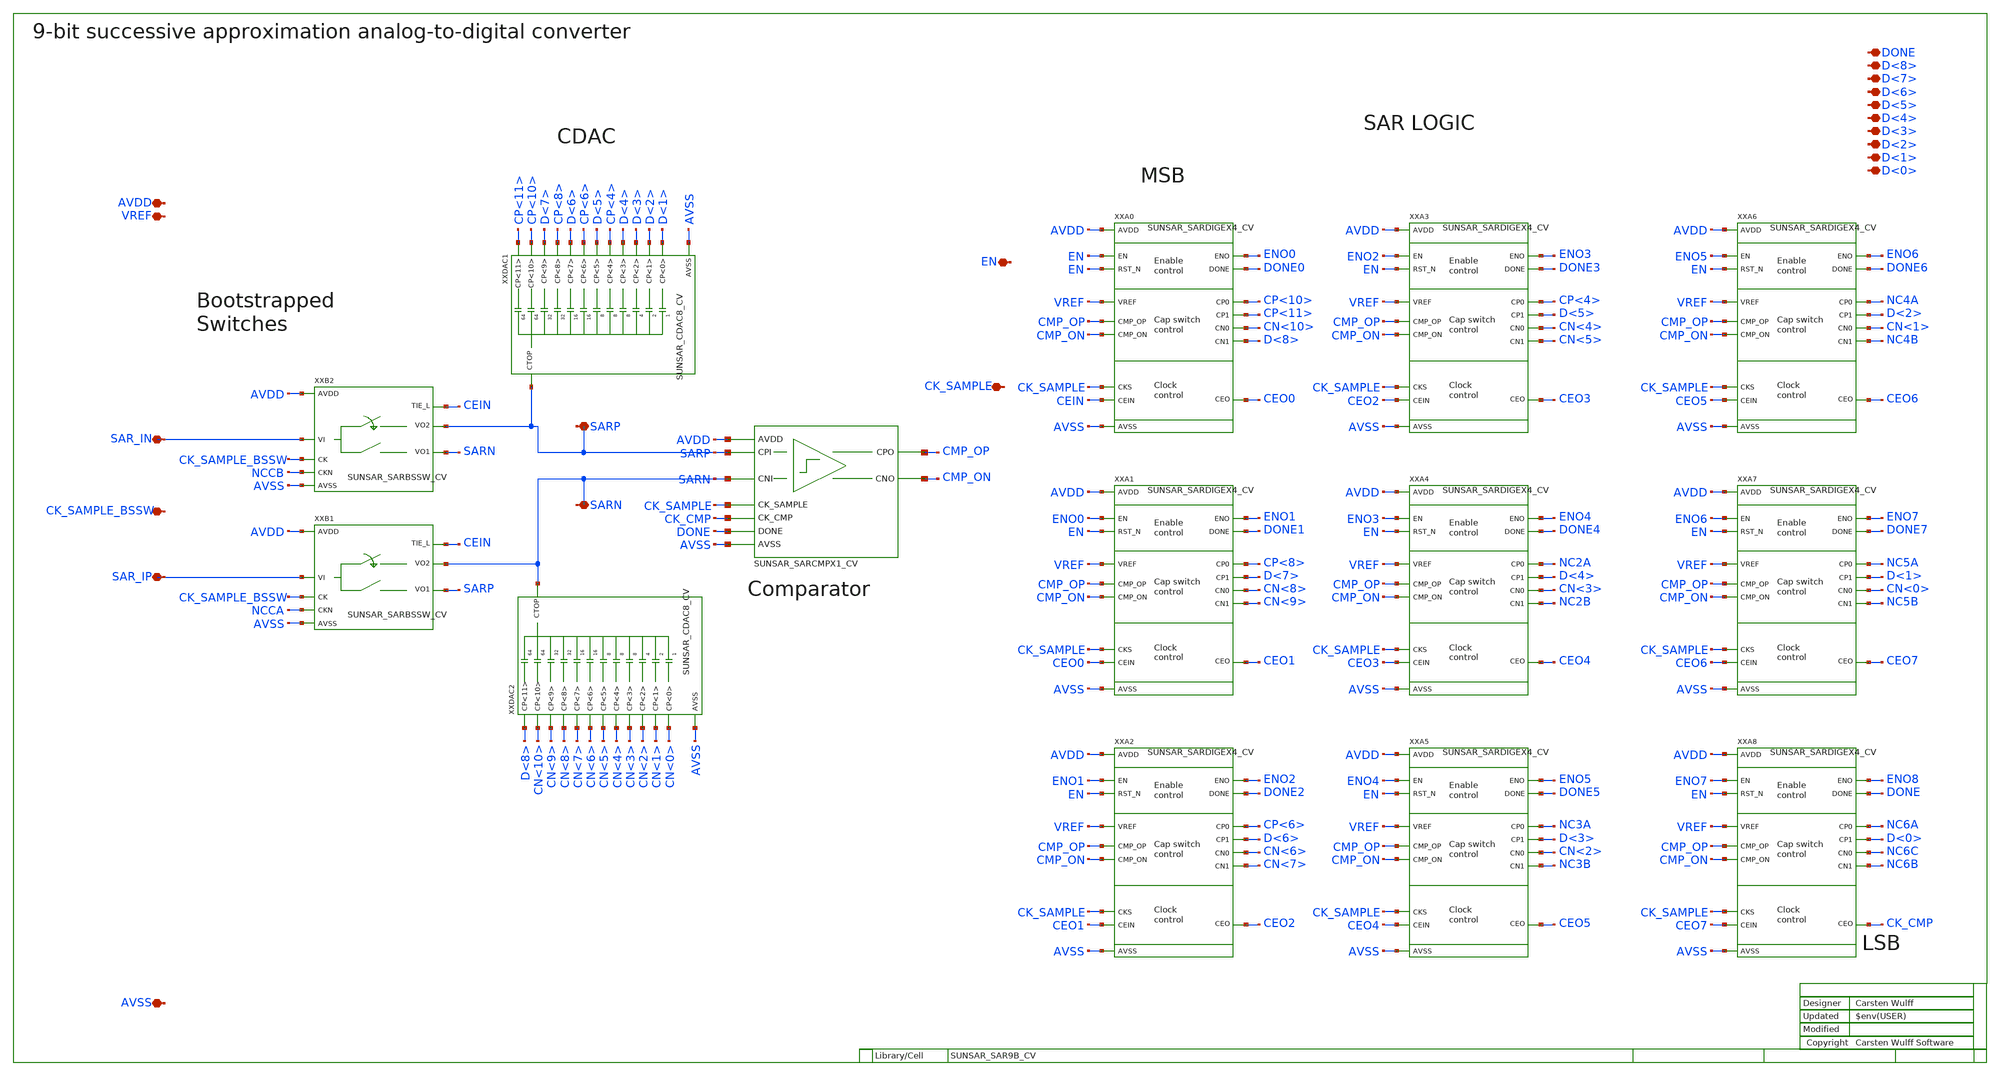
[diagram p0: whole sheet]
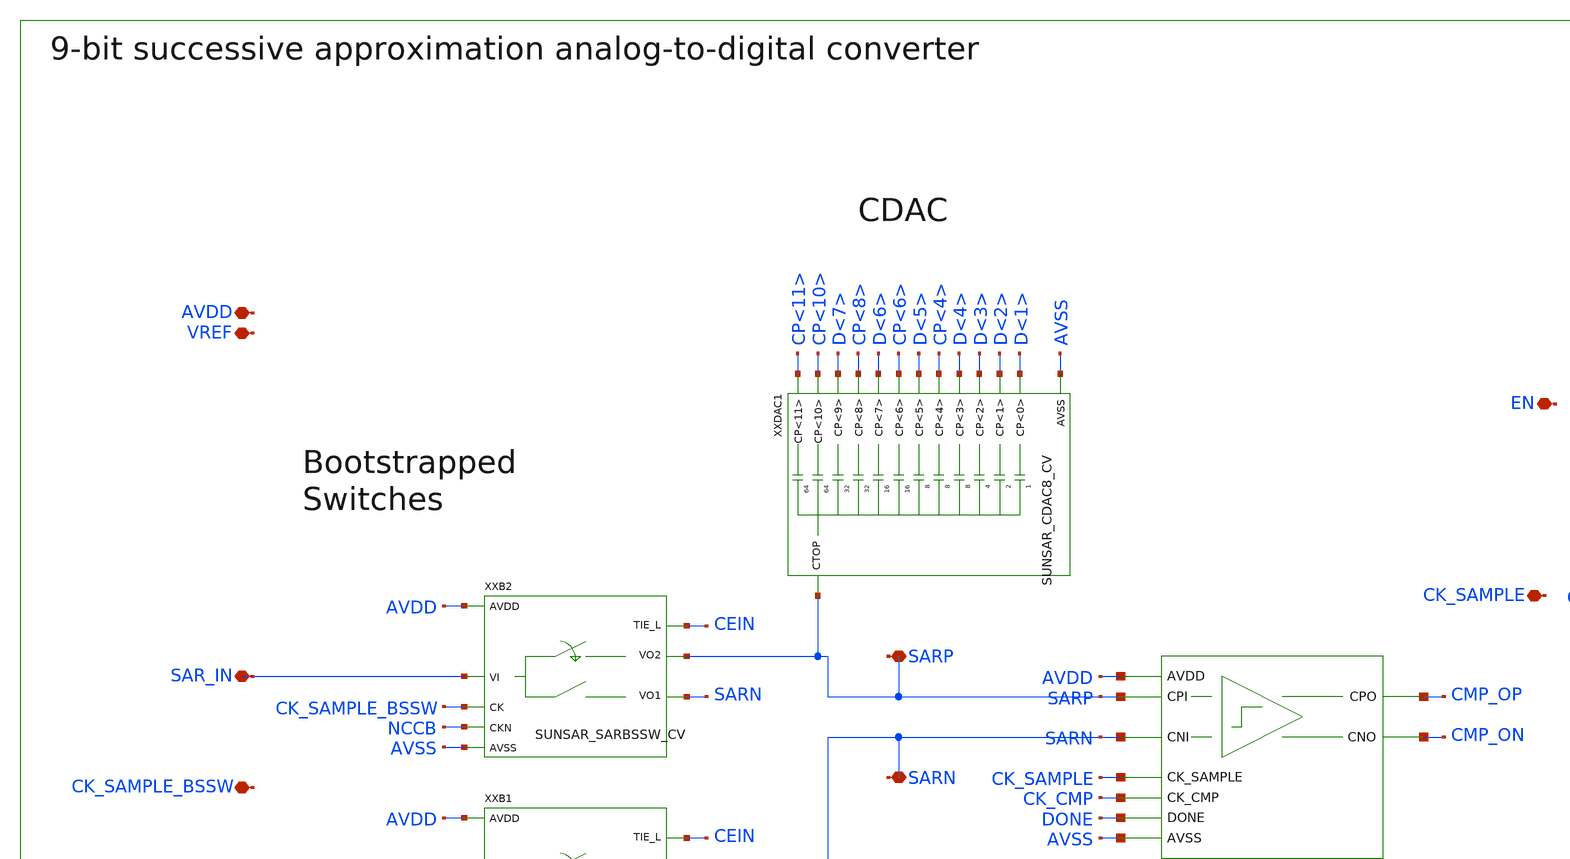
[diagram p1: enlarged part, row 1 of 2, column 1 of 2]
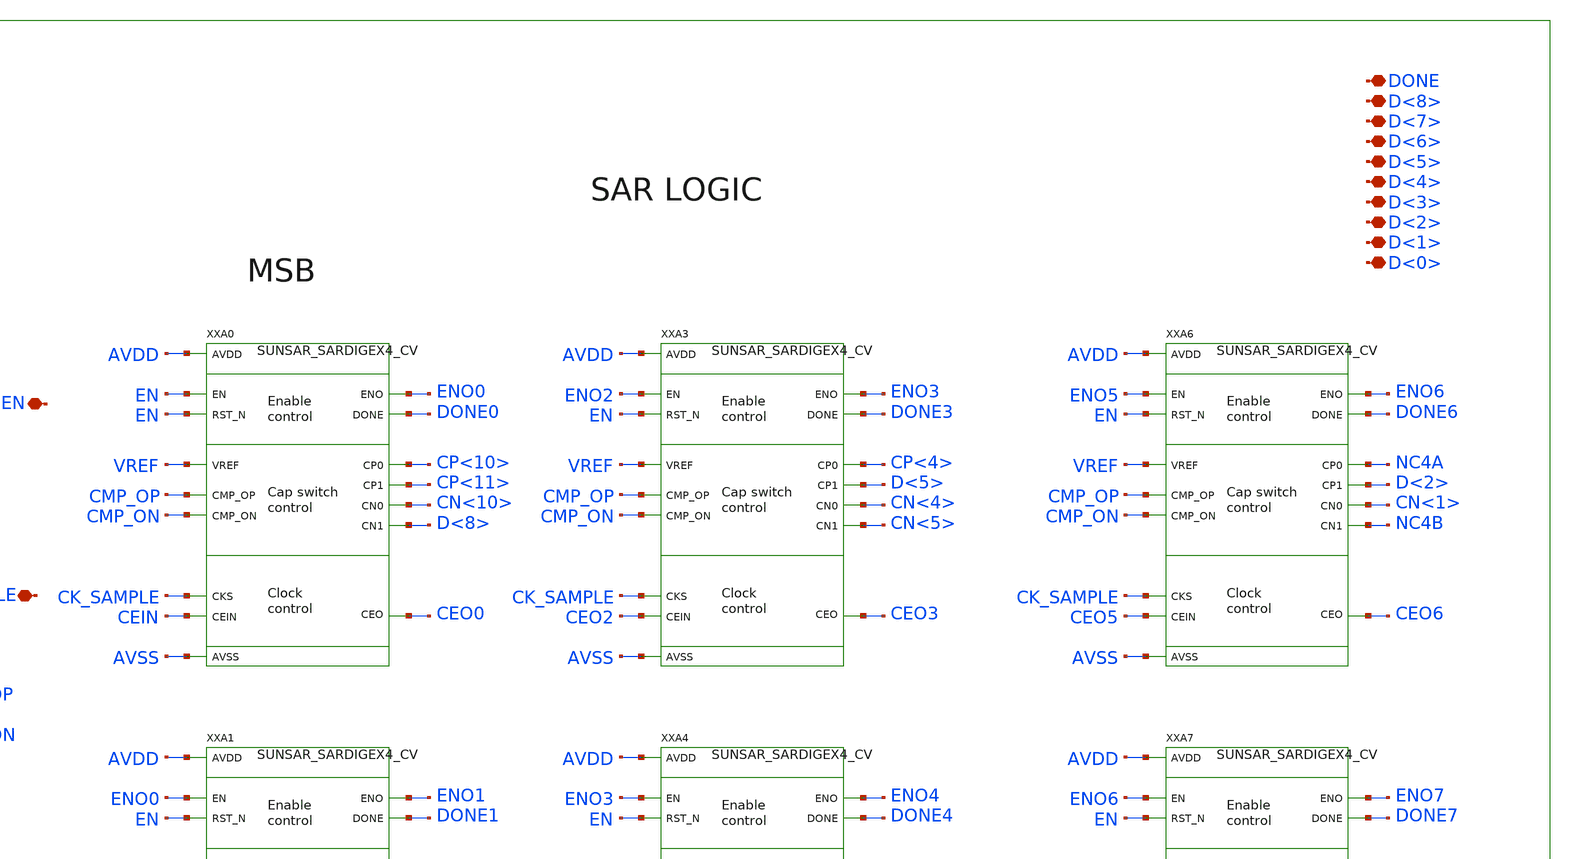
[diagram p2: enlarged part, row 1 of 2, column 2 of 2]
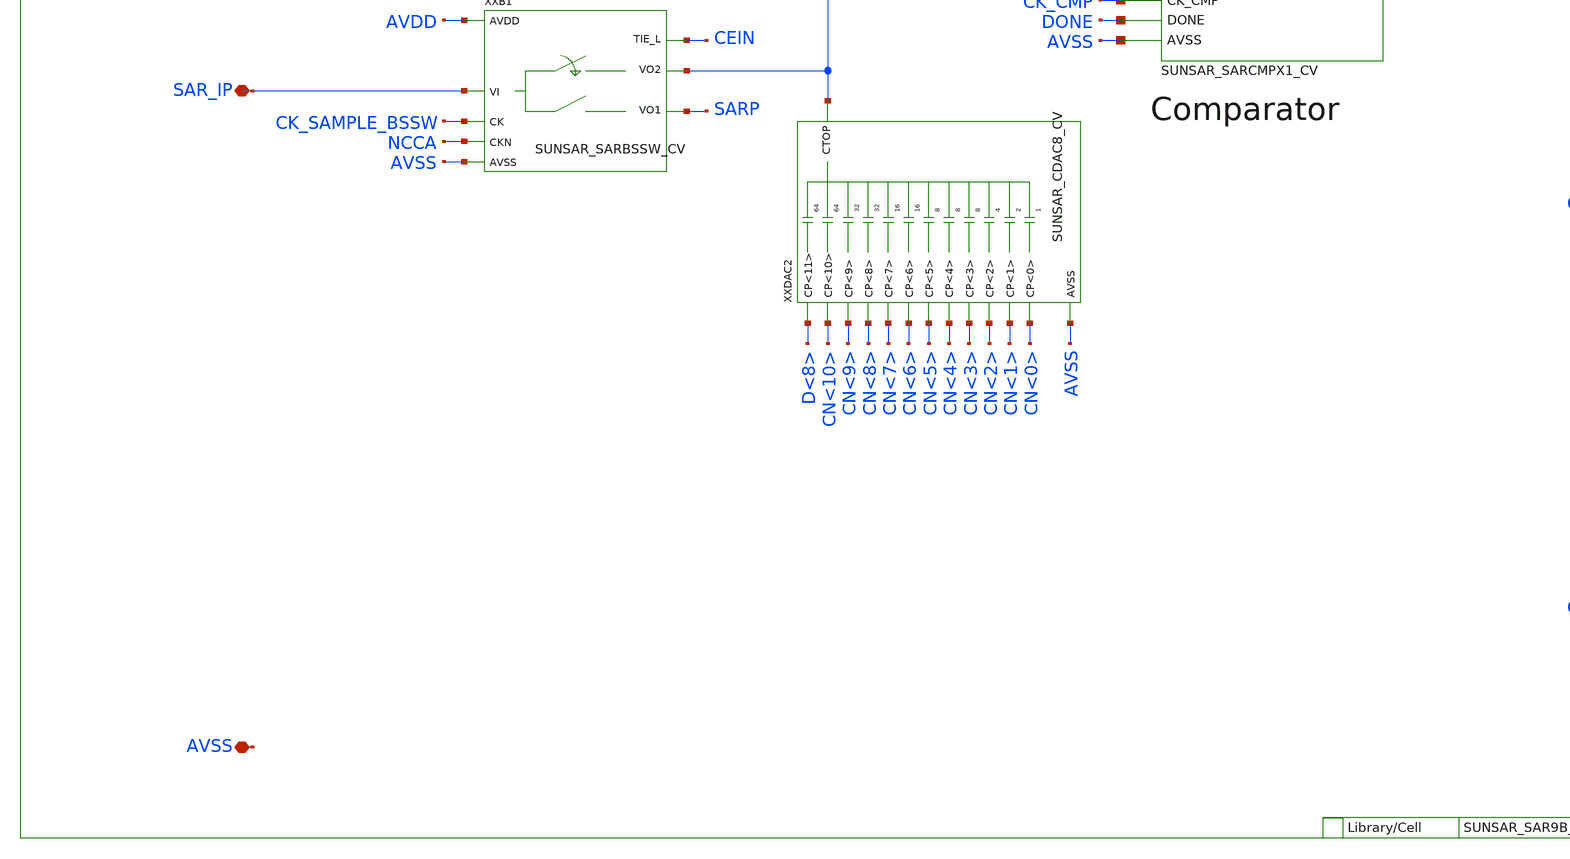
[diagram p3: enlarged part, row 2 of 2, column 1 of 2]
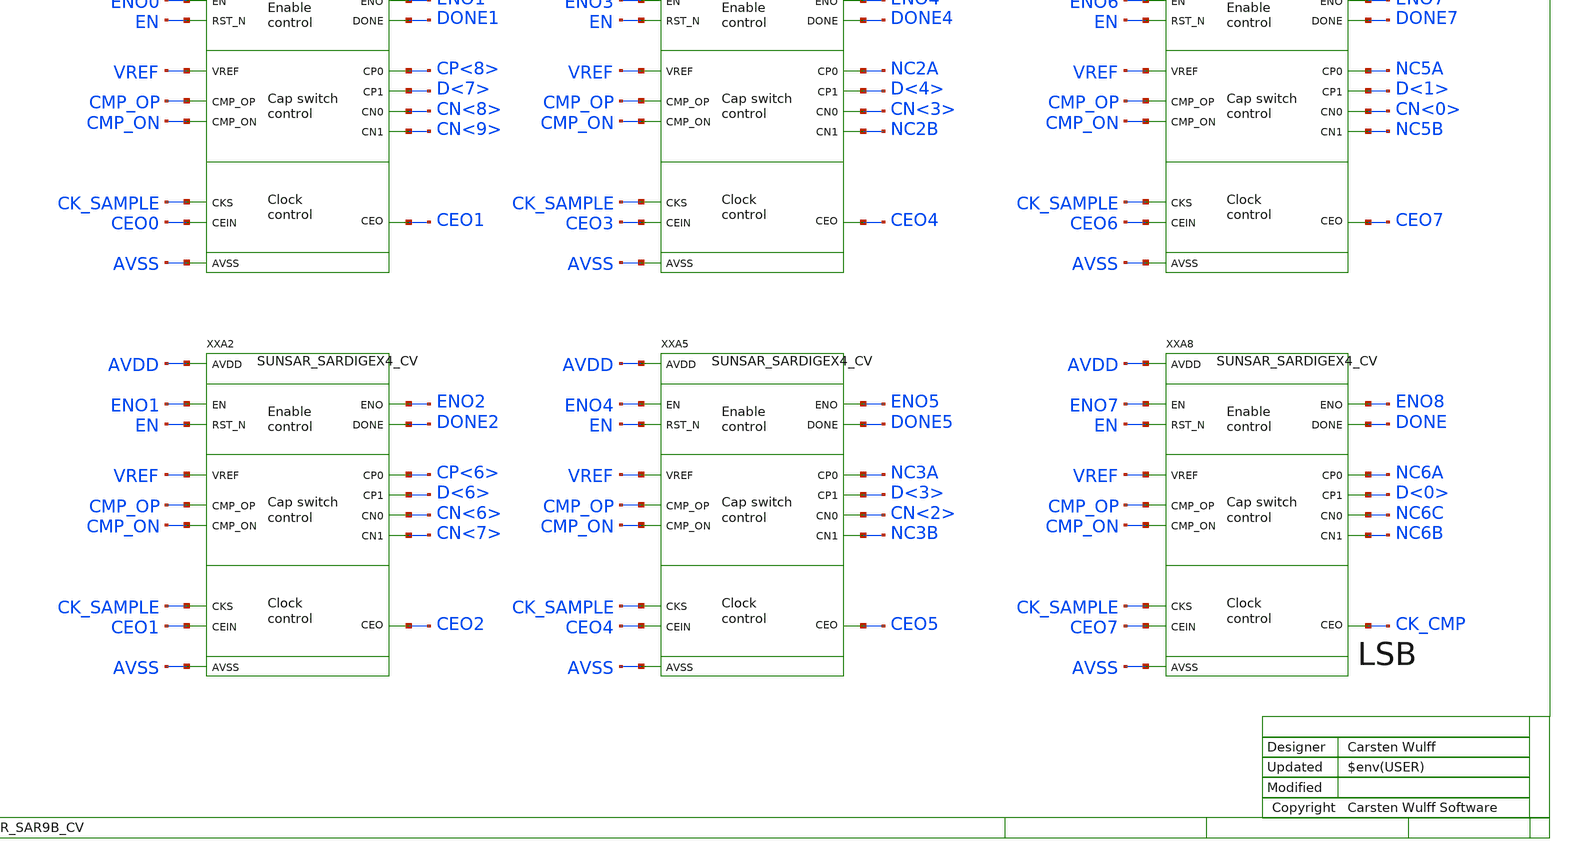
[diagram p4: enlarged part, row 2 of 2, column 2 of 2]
** sch_path: ip/sun_sar9b_sky130nm/design/SUN_SAR9B_SKY130NM/SUNSAR_SAR9B_CV.sch
**.subckt SUNSAR_SAR9B_CV SAR_IP SAR_IN SARN SARP DONE D<8> D<7> D<6> D<5> D<4> D<3> D<2> D<1> D<0>
*+ EN CK_SAMPLE CK_SAMPLE_BSSW VREF AVDD AVSS
*.iopin SAR_IP
*.iopin SAR_IN
*.iopin SARN
*.iopin SARP
*.iopin DONE
*.iopin D<8>
*.iopin D<7>
*.iopin D<6>
*.iopin D<5>
*.iopin D<4>
*.iopin D<3>
*.iopin D<2>
*.iopin D<1>
*.iopin D<0>
*.iopin EN
*.iopin CK_SAMPLE
*.iopin CK_SAMPLE_BSSW
*.iopin VREF
*.iopin AVDD
*.iopin AVSS
XXB1 SAR_IP CK_SAMPLE_BSSW NCCA CEIN SARP SARN AVDD AVSS SUNSAR_SARBSSW_CV
XXB2 SAR_IN CK_SAMPLE_BSSW NCCB CEIN SARN SARP AVDD AVSS SUNSAR_SARBSSW_CV
XXDAC1 CP<11> CP<10> D<7> CP<8> D<6> CP<6> D<5> CP<4> D<4> D<3> D<2> D<1> SARP AVSS SUNSAR_CDAC8_CV
XXDAC2 D<8> CN<10> CN<9> CN<8> CN<7> CN<6> CN<5> CN<4> CN<3> CN<2> CN<1> CN<0> SARN AVSS
+ SUNSAR_CDAC8_CV
XXA0 CMP_OP CMP_ON EN EN ENO0 DONE0 CP<10> CP<11> CN<10> D<8> CEIN CEO0 CK_SAMPLE VREF AVDD AVSS
+ SUNSAR_SARDIGEX4_CV
XXA1 CMP_OP CMP_ON ENO0 EN ENO1 DONE1 CP<8> D<7> CN<8> CN<9> CEO0 CEO1 CK_SAMPLE VREF AVDD AVSS
+ SUNSAR_SARDIGEX4_CV
XXA2 CMP_OP CMP_ON ENO1 EN ENO2 DONE2 CP<6> D<6> CN<6> CN<7> CEO1 CEO2 CK_SAMPLE VREF AVDD AVSS
+ SUNSAR_SARDIGEX4_CV
XXA3 CMP_OP CMP_ON ENO2 EN ENO3 DONE3 CP<4> D<5> CN<4> CN<5> CEO2 CEO3 CK_SAMPLE VREF AVDD AVSS
+ SUNSAR_SARDIGEX4_CV
XXA4 CMP_OP CMP_ON ENO3 EN ENO4 DONE4 NC2A D<4> CN<3> NC2B CEO3 CEO4 CK_SAMPLE VREF AVDD AVSS
+ SUNSAR_SARDIGEX4_CV
XXA5 CMP_OP CMP_ON ENO4 EN ENO5 DONE5 NC3A D<3> CN<2> NC3B CEO4 CEO5 CK_SAMPLE VREF AVDD AVSS
+ SUNSAR_SARDIGEX4_CV
XXA6 CMP_OP CMP_ON ENO5 EN ENO6 DONE6 NC4A D<2> CN<1> NC4B CEO5 CEO6 CK_SAMPLE VREF AVDD AVSS
+ SUNSAR_SARDIGEX4_CV
XXA7 CMP_OP CMP_ON ENO6 EN ENO7 DONE7 NC5A D<1> CN<0> NC5B CEO6 CEO7 CK_SAMPLE VREF AVDD AVSS
+ SUNSAR_SARDIGEX4_CV
XXA8 CMP_OP CMP_ON ENO7 EN ENO8 DONE NC6A D<0> NC6C NC6B CEO7 CK_CMP CK_SAMPLE VREF AVDD AVSS
+ SUNSAR_SARDIGEX4_CV
XXA20 SARP SARN CMP_OP CMP_ON CK_CMP CK_SAMPLE DONE AVDD AVSS SUNSAR_SARCMPX1_CV
**.ends
.end
